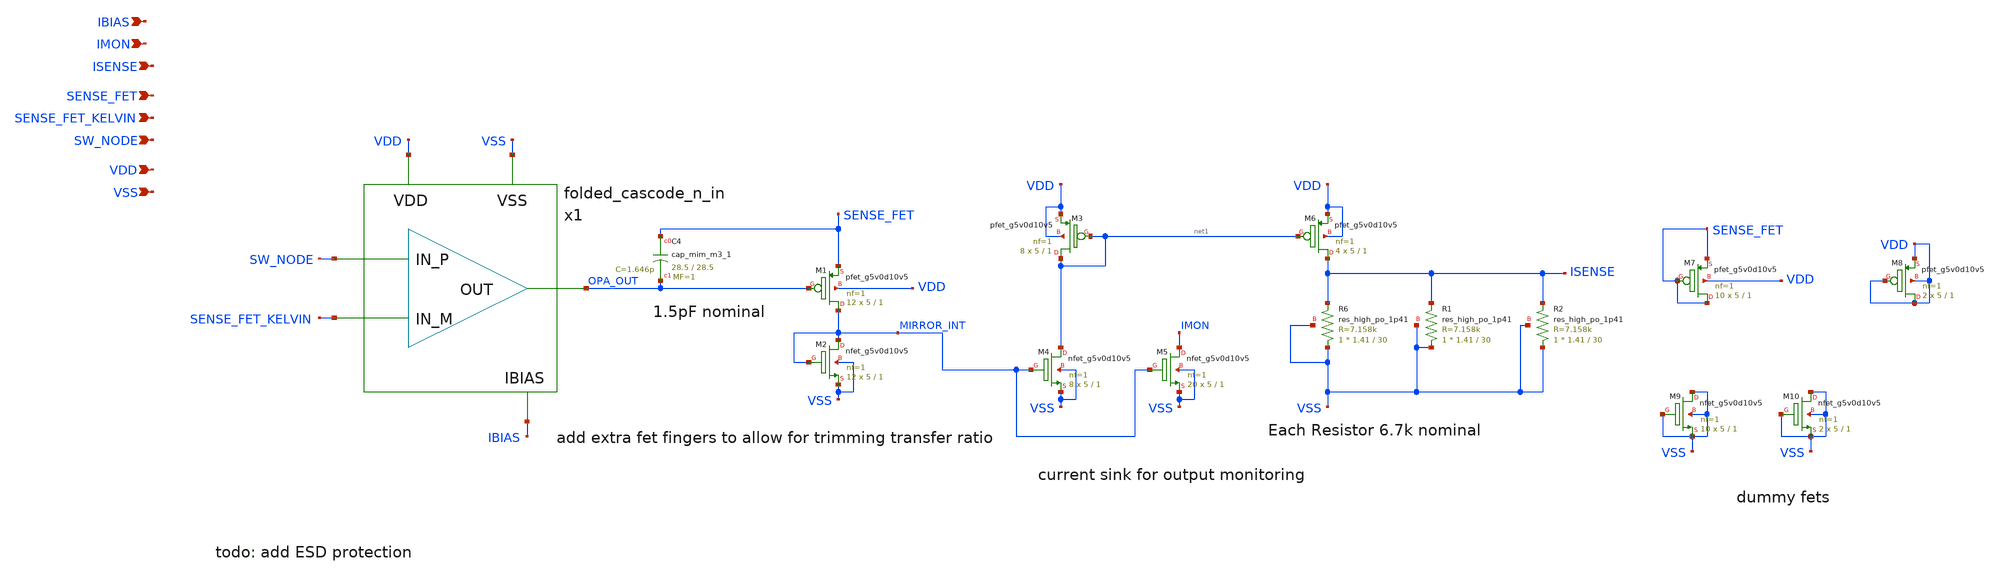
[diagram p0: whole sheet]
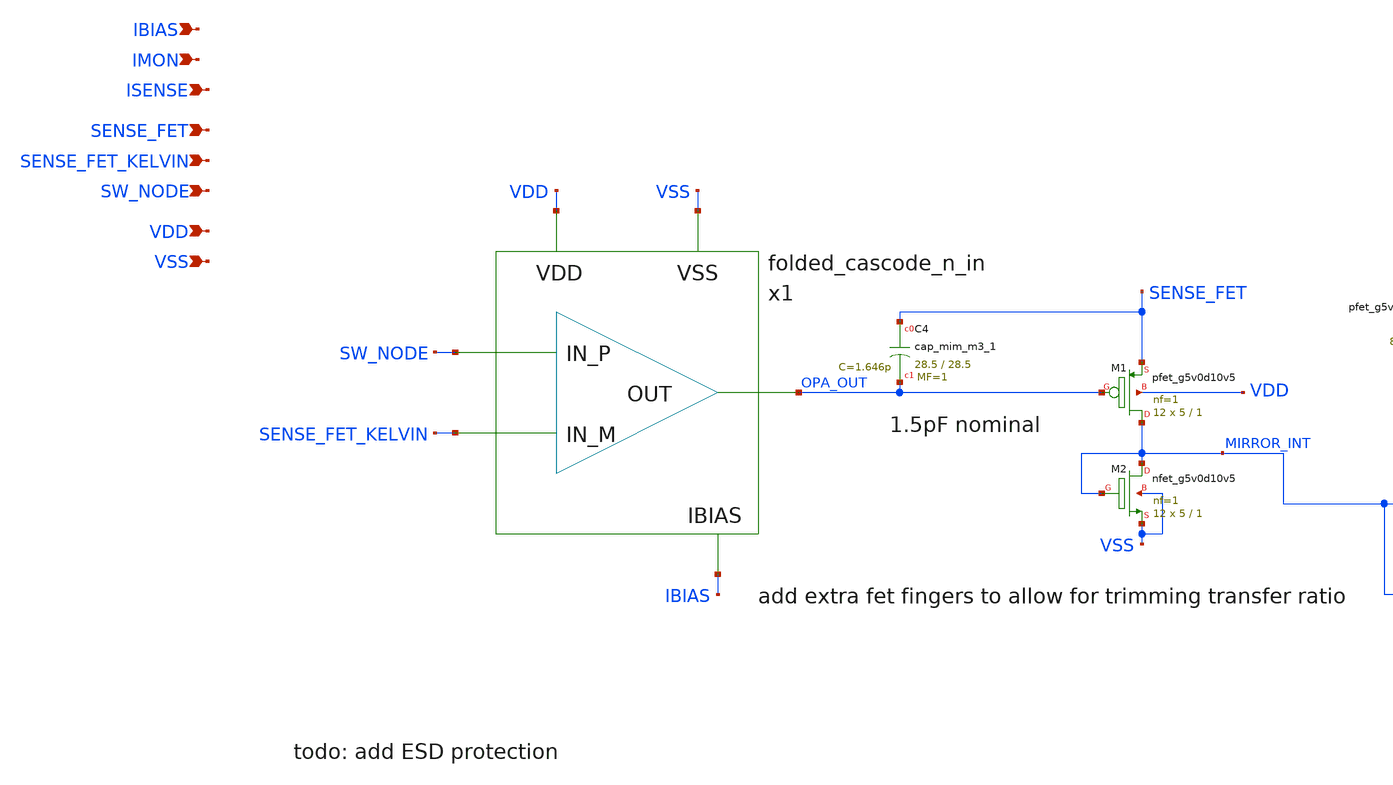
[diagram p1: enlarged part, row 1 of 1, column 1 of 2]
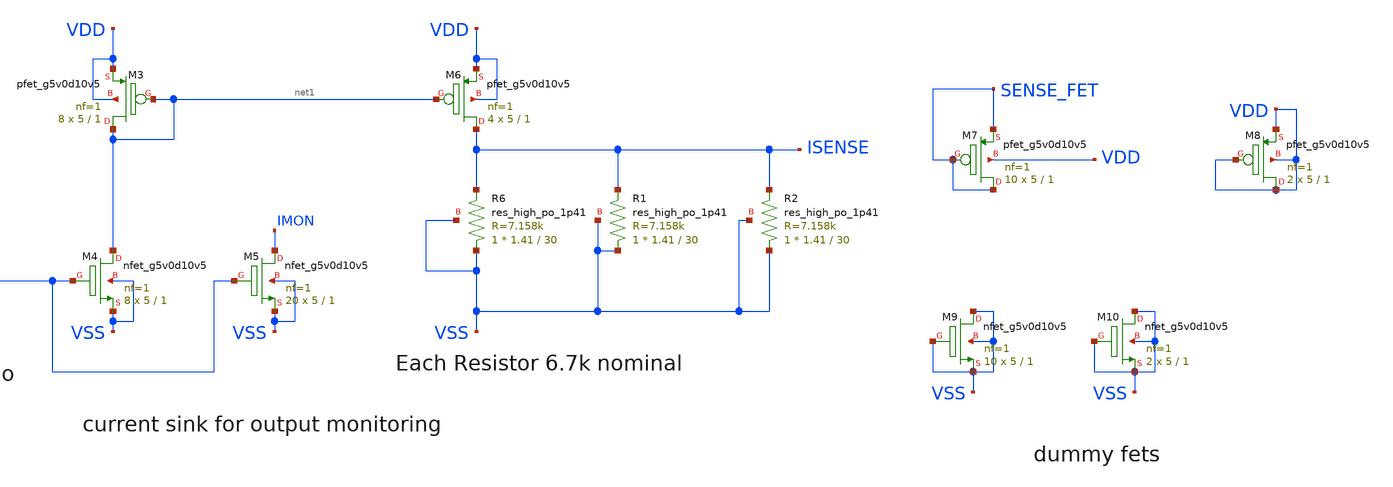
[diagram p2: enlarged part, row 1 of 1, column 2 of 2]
** sch_path: images/foss-asic-tools/addons/examples/open-pmic/design/current-sense/current_sense.sch
**.subckt current_sense IBIAS IMON ISENSE SENSE_FET SENSE_FET_KELVIN SW_NODE VDD VSS
*.ipin IBIAS
*.ipin IMON
*.ipin ISENSE
*.ipin SENSE_FET
*.ipin SENSE_FET_KELVIN
*.ipin SW_NODE
*.ipin VDD
*.ipin VSS
x1 SW_NODE SENSE_FET_KELVIN OPA_OUT VDD VSS IBIAS folded_cascode_n_in
XM1 MIRROR_INT OPA_OUT SENSE_FET VDD sky130_fd_pr__pfet_g5v0d10v5 L=1 W=5 nf=1 ad='int((nf+1)/2) * W/nf * 0.29'
+ as='int((nf+2)/2) * W/nf * 0.29' pd='2*int((nf+1)/2) * (W/nf + 0.29)' ps='2*int((nf+2)/2) * (W/nf + 0.29)'
+ nrd='0.29 / W' nrs='0.29 / W' sa=0 sb=0 sd=0 mult=12 m=12
XM2 MIRROR_INT MIRROR_INT VSS VSS sky130_fd_pr__nfet_g5v0d10v5 L=1 W=5 nf=1 ad='int((nf+1)/2) * W/nf * 0.29'
+ as='int((nf+2)/2) * W/nf * 0.29' pd='2*int((nf+1)/2) * (W/nf + 0.29)' ps='2*int((nf+2)/2) * (W/nf + 0.29)'
+ nrd='0.29 / W' nrs='0.29 / W' sa=0 sb=0 sd=0 mult=12 m=12
XM4 net1 MIRROR_INT VSS VSS sky130_fd_pr__nfet_g5v0d10v5 L=1 W=5 nf=1 ad='int((nf+1)/2) * W/nf * 0.29'
+ as='int((nf+2)/2) * W/nf * 0.29' pd='2*int((nf+1)/2) * (W/nf + 0.29)' ps='2*int((nf+2)/2) * (W/nf + 0.29)'
+ nrd='0.29 / W' nrs='0.29 / W' sa=0 sb=0 sd=0 mult=8 m=8
XM3 net1 net1 VDD VDD sky130_fd_pr__pfet_g5v0d10v5 L=1 W=5 nf=1 ad='int((nf+1)/2) * W/nf * 0.29' as='int((nf+2)/2) * W/nf * 0.29'
+ pd='2*int((nf+1)/2) * (W/nf + 0.29)' ps='2*int((nf+2)/2) * (W/nf + 0.29)' nrd='0.29 / W' nrs='0.29 / W'
+ sa=0 sb=0 sd=0 mult=8 m=8
XM5 IMON MIRROR_INT VSS VSS sky130_fd_pr__nfet_g5v0d10v5 L=1 W=5 nf=1 ad='int((nf+1)/2) * W/nf * 0.29'
+ as='int((nf+2)/2) * W/nf * 0.29' pd='2*int((nf+1)/2) * (W/nf + 0.29)' ps='2*int((nf+2)/2) * (W/nf + 0.29)'
+ nrd='0.29 / W' nrs='0.29 / W' sa=0 sb=0 sd=0 mult=20 m=20
XM6 ISENSE net1 VDD VDD sky130_fd_pr__pfet_g5v0d10v5 L=1 W=5 nf=1 ad='int((nf+1)/2) * W/nf * 0.29' as='int((nf+2)/2) * W/nf * 0.29'
+ pd='2*int((nf+1)/2) * (W/nf + 0.29)' ps='2*int((nf+2)/2) * (W/nf + 0.29)' nrd='0.29 / W' nrs='0.29 / W'
+ sa=0 sb=0 sd=0 mult=4 m=4
XR6 VSS ISENSE VSS sky130_fd_pr__res_high_po_1p41 L=30 mult=1 m=1
XR1 VSS ISENSE VSS sky130_fd_pr__res_high_po_1p41 L=30 mult=1 m=1
XC4 SENSE_FET OPA_OUT sky130_fd_pr__cap_mim_m3_1 W=28.5 L=28.5 MF=1 m=1
XR2 VSS ISENSE VSS sky130_fd_pr__res_high_po_1p41 L=30 mult=1 m=1
XM7 SENSE_FET SENSE_FET SENSE_FET VDD sky130_fd_pr__pfet_g5v0d10v5 L=1 W=5 nf=1 ad='int((nf+1)/2) * W/nf * 0.29'
+ as='int((nf+2)/2) * W/nf * 0.29' pd='2*int((nf+1)/2) * (W/nf + 0.29)' ps='2*int((nf+2)/2) * (W/nf + 0.29)'
+ nrd='0.29 / W' nrs='0.29 / W' sa=0 sb=0 sd=0 mult=10 m=10
XM8 VDD VDD VDD VDD sky130_fd_pr__pfet_g5v0d10v5 L=1 W=5 nf=1 ad='int((nf+1)/2) * W/nf * 0.29' as='int((nf+2)/2) * W/nf * 0.29'
+ pd='2*int((nf+1)/2) * (W/nf + 0.29)' ps='2*int((nf+2)/2) * (W/nf + 0.29)' nrd='0.29 / W' nrs='0.29 / W'
+ sa=0 sb=0 sd=0 mult=2 m=2
XM9 VSS VSS VSS VSS sky130_fd_pr__nfet_g5v0d10v5 L=1 W=5 nf=1 ad='int((nf+1)/2) * W/nf * 0.29' as='int((nf+2)/2) * W/nf * 0.29'
+ pd='2*int((nf+1)/2) * (W/nf + 0.29)' ps='2*int((nf+2)/2) * (W/nf + 0.29)' nrd='0.29 / W' nrs='0.29 / W'
+ sa=0 sb=0 sd=0 mult=10 m=10
XM10 VSS VSS VSS VSS sky130_fd_pr__nfet_g5v0d10v5 L=1 W=5 nf=1 ad='int((nf+1)/2) * W/nf * 0.29' as='int((nf+2)/2) * W/nf * 0.29'
+ pd='2*int((nf+1)/2) * (W/nf + 0.29)' ps='2*int((nf+2)/2) * (W/nf + 0.29)' nrd='0.29 / W' nrs='0.29 / W'
+ sa=0 sb=0 sd=0 mult=2 m=2
**.ends
.end
